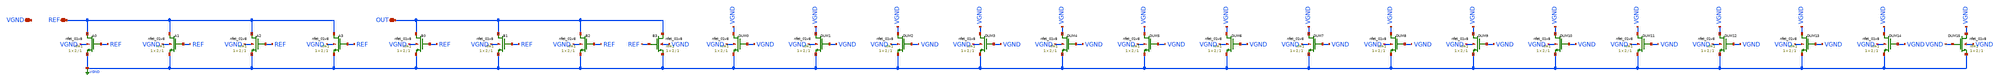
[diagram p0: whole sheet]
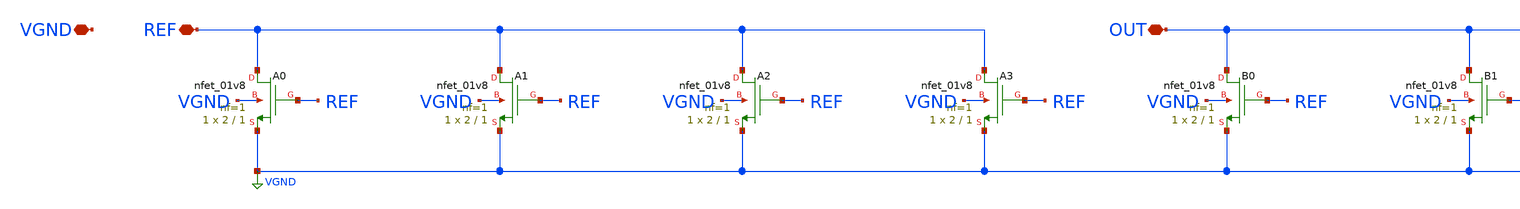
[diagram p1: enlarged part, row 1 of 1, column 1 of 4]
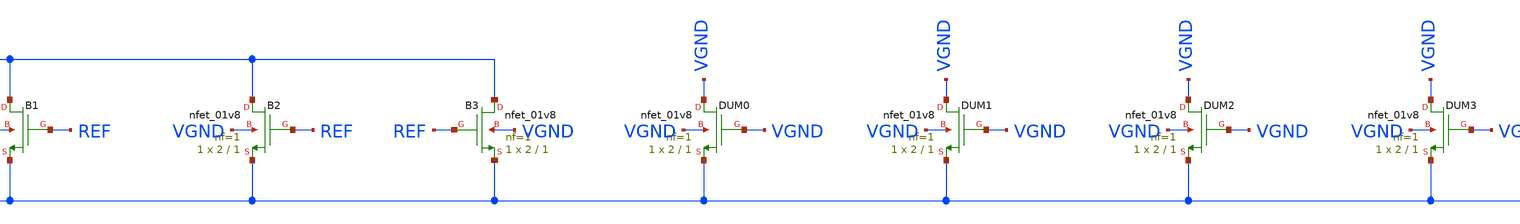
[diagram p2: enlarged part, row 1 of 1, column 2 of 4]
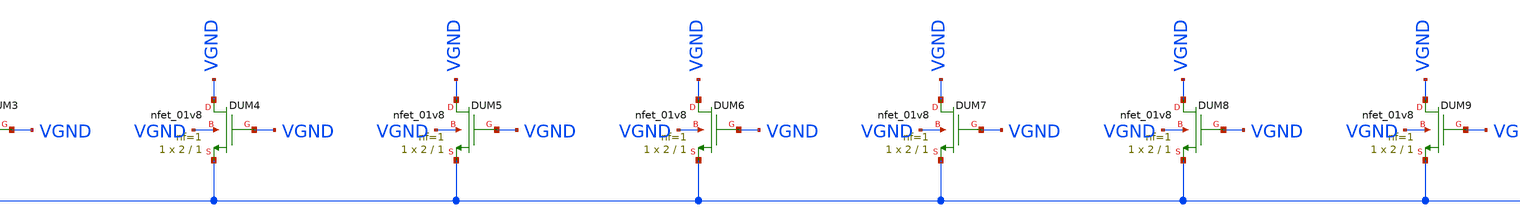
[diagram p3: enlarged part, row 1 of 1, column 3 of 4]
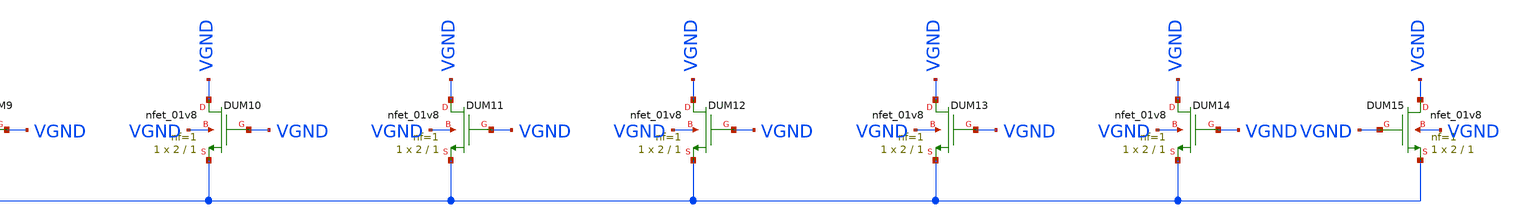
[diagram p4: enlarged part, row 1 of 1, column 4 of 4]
** sch_path: cells/ELAD1_MIRROR_GROUPED/schematic/ELAD1_MIRROR_GROUPED.sch
**.subckt ELAD1_MIRROR_GROUPED REF OUT VGND
*.iopin REF
*.iopin OUT
*.iopin VGND
XA0 REF REF VGND VGND sky130_fd_pr__nfet_01v8 L=1 W=2 nf=1 ad='int((1 + 1)/2) * 2 / 1 * 0.29' as='int((1 + 2)/2) * 2 / 1 * 0.29'
+ pd='2*int((1 + 1)/2) * (2 / 1 + 0.29)' ps='2*int((1 + 2)/2) * (2 / 1 + 0.29)' nrd='0.29 / 2 ' nrs='0.29 / 2 '
+ sa=0 sb=0 sd=0 mult=1 m=1
XA1 REF REF VGND VGND sky130_fd_pr__nfet_01v8 L=1 W=2 nf=1 ad='int((1 + 1)/2) * 2 / 1 * 0.29' as='int((1 + 2)/2) * 2 / 1 * 0.29'
+ pd='2*int((1 + 1)/2) * (2 / 1 + 0.29)' ps='2*int((1 + 2)/2) * (2 / 1 + 0.29)' nrd='0.29 / 2 ' nrs='0.29 / 2 '
+ sa=0 sb=0 sd=0 mult=1 m=1
XA2 REF REF VGND VGND sky130_fd_pr__nfet_01v8 L=1 W=2 nf=1 ad='int((1 + 1)/2) * 2 / 1 * 0.29' as='int((1 + 2)/2) * 2 / 1 * 0.29'
+ pd='2*int((1 + 1)/2) * (2 / 1 + 0.29)' ps='2*int((1 + 2)/2) * (2 / 1 + 0.29)' nrd='0.29 / 2 ' nrs='0.29 / 2 '
+ sa=0 sb=0 sd=0 mult=1 m=1
XA3 REF REF VGND VGND sky130_fd_pr__nfet_01v8 L=1 W=2 nf=1 ad='int((1 + 1)/2) * 2 / 1 * 0.29' as='int((1 + 2)/2) * 2 / 1 * 0.29'
+ pd='2*int((1 + 1)/2) * (2 / 1 + 0.29)' ps='2*int((1 + 2)/2) * (2 / 1 + 0.29)' nrd='0.29 / 2 ' nrs='0.29 / 2 '
+ sa=0 sb=0 sd=0 mult=1 m=1
XB0 OUT REF VGND VGND sky130_fd_pr__nfet_01v8 L=1 W=2 nf=1 ad='int((1 + 1)/2) * 2 / 1 * 0.29' as='int((1 + 2)/2) * 2 / 1 * 0.29'
+ pd='2*int((1 + 1)/2) * (2 / 1 + 0.29)' ps='2*int((1 + 2)/2) * (2 / 1 + 0.29)' nrd='0.29 / 2 ' nrs='0.29 / 2 '
+ sa=0 sb=0 sd=0 mult=1 m=1
XB1 OUT REF VGND VGND sky130_fd_pr__nfet_01v8 L=1 W=2 nf=1 ad='int((1 + 1)/2) * 2 / 1 * 0.29' as='int((1 + 2)/2) * 2 / 1 * 0.29'
+ pd='2*int((1 + 1)/2) * (2 / 1 + 0.29)' ps='2*int((1 + 2)/2) * (2 / 1 + 0.29)' nrd='0.29 / 2 ' nrs='0.29 / 2 '
+ sa=0 sb=0 sd=0 mult=1 m=1
XB2 OUT REF VGND VGND sky130_fd_pr__nfet_01v8 L=1 W=2 nf=1 ad='int((1 + 1)/2) * 2 / 1 * 0.29' as='int((1 + 2)/2) * 2 / 1 * 0.29'
+ pd='2*int((1 + 1)/2) * (2 / 1 + 0.29)' ps='2*int((1 + 2)/2) * (2 / 1 + 0.29)' nrd='0.29 / 2 ' nrs='0.29 / 2 '
+ sa=0 sb=0 sd=0 mult=1 m=1
XB3 OUT REF VGND VGND sky130_fd_pr__nfet_01v8 L=1 W=2 nf=1 ad='int((1 + 1)/2) * 2 / 1 * 0.29' as='int((1 + 2)/2) * 2 / 1 * 0.29'
+ pd='2*int((1 + 1)/2) * (2 / 1 + 0.29)' ps='2*int((1 + 2)/2) * (2 / 1 + 0.29)' nrd='0.29 / 2 ' nrs='0.29 / 2 '
+ sa=0 sb=0 sd=0 mult=1 m=1
XDUM0 VGND VGND VGND VGND sky130_fd_pr__nfet_01v8 L=1 W=2 nf=1 ad='int((1 + 1)/2) * 2 / 1 * 0.29' as='int((1 + 2)/2) * 2 / 1 * 0.29'
+ pd='2*int((1 + 1)/2) * (2 / 1 + 0.29)' ps='2*int((1 + 2)/2) * (2 / 1 + 0.29)' nrd='0.29 / 2 ' nrs='0.29 / 2 '
+ sa=0 sb=0 sd=0 mult=1 m=1
XDUM1 VGND VGND VGND VGND sky130_fd_pr__nfet_01v8 L=1 W=2 nf=1 ad='int((1 + 1)/2) * 2 / 1 * 0.29' as='int((1 + 2)/2) * 2 / 1 * 0.29'
+ pd='2*int((1 + 1)/2) * (2 / 1 + 0.29)' ps='2*int((1 + 2)/2) * (2 / 1 + 0.29)' nrd='0.29 / 2 ' nrs='0.29 / 2 '
+ sa=0 sb=0 sd=0 mult=1 m=1
XDUM2 VGND VGND VGND VGND sky130_fd_pr__nfet_01v8 L=1 W=2 nf=1 ad='int((1 + 1)/2) * 2 / 1 * 0.29' as='int((1 + 2)/2) * 2 / 1 * 0.29'
+ pd='2*int((1 + 1)/2) * (2 / 1 + 0.29)' ps='2*int((1 + 2)/2) * (2 / 1 + 0.29)' nrd='0.29 / 2 ' nrs='0.29 / 2 '
+ sa=0 sb=0 sd=0 mult=1 m=1
XDUM3 VGND VGND VGND VGND sky130_fd_pr__nfet_01v8 L=1 W=2 nf=1 ad='int((1 + 1)/2) * 2 / 1 * 0.29' as='int((1 + 2)/2) * 2 / 1 * 0.29'
+ pd='2*int((1 + 1)/2) * (2 / 1 + 0.29)' ps='2*int((1 + 2)/2) * (2 / 1 + 0.29)' nrd='0.29 / 2 ' nrs='0.29 / 2 '
+ sa=0 sb=0 sd=0 mult=1 m=1
XDUM4 VGND VGND VGND VGND sky130_fd_pr__nfet_01v8 L=1 W=2 nf=1 ad='int((1 + 1)/2) * 2 / 1 * 0.29' as='int((1 + 2)/2) * 2 / 1 * 0.29'
+ pd='2*int((1 + 1)/2) * (2 / 1 + 0.29)' ps='2*int((1 + 2)/2) * (2 / 1 + 0.29)' nrd='0.29 / 2 ' nrs='0.29 / 2 '
+ sa=0 sb=0 sd=0 mult=1 m=1
XDUM5 VGND VGND VGND VGND sky130_fd_pr__nfet_01v8 L=1 W=2 nf=1 ad='int((1 + 1)/2) * 2 / 1 * 0.29' as='int((1 + 2)/2) * 2 / 1 * 0.29'
+ pd='2*int((1 + 1)/2) * (2 / 1 + 0.29)' ps='2*int((1 + 2)/2) * (2 / 1 + 0.29)' nrd='0.29 / 2 ' nrs='0.29 / 2 '
+ sa=0 sb=0 sd=0 mult=1 m=1
XDUM6 VGND VGND VGND VGND sky130_fd_pr__nfet_01v8 L=1 W=2 nf=1 ad='int((1 + 1)/2) * 2 / 1 * 0.29' as='int((1 + 2)/2) * 2 / 1 * 0.29'
+ pd='2*int((1 + 1)/2) * (2 / 1 + 0.29)' ps='2*int((1 + 2)/2) * (2 / 1 + 0.29)' nrd='0.29 / 2 ' nrs='0.29 / 2 '
+ sa=0 sb=0 sd=0 mult=1 m=1
XDUM7 VGND VGND VGND VGND sky130_fd_pr__nfet_01v8 L=1 W=2 nf=1 ad='int((1 + 1)/2) * 2 / 1 * 0.29' as='int((1 + 2)/2) * 2 / 1 * 0.29'
+ pd='2*int((1 + 1)/2) * (2 / 1 + 0.29)' ps='2*int((1 + 2)/2) * (2 / 1 + 0.29)' nrd='0.29 / 2 ' nrs='0.29 / 2 '
+ sa=0 sb=0 sd=0 mult=1 m=1
XDUM8 VGND VGND VGND VGND sky130_fd_pr__nfet_01v8 L=1 W=2 nf=1 ad='int((1 + 1)/2) * 2 / 1 * 0.29' as='int((1 + 2)/2) * 2 / 1 * 0.29'
+ pd='2*int((1 + 1)/2) * (2 / 1 + 0.29)' ps='2*int((1 + 2)/2) * (2 / 1 + 0.29)' nrd='0.29 / 2 ' nrs='0.29 / 2 '
+ sa=0 sb=0 sd=0 mult=1 m=1
XDUM9 VGND VGND VGND VGND sky130_fd_pr__nfet_01v8 L=1 W=2 nf=1 ad='int((1 + 1)/2) * 2 / 1 * 0.29' as='int((1 + 2)/2) * 2 / 1 * 0.29'
+ pd='2*int((1 + 1)/2) * (2 / 1 + 0.29)' ps='2*int((1 + 2)/2) * (2 / 1 + 0.29)' nrd='0.29 / 2 ' nrs='0.29 / 2 '
+ sa=0 sb=0 sd=0 mult=1 m=1
XDUM10 VGND VGND VGND VGND sky130_fd_pr__nfet_01v8 L=1 W=2 nf=1 ad='int((1 + 1)/2) * 2 / 1 * 0.29' as='int((1 + 2)/2) * 2 / 1 * 0.29'
+ pd='2*int((1 + 1)/2) * (2 / 1 + 0.29)' ps='2*int((1 + 2)/2) * (2 / 1 + 0.29)' nrd='0.29 / 2 ' nrs='0.29 / 2 '
+ sa=0 sb=0 sd=0 mult=1 m=1
XDUM11 VGND VGND VGND VGND sky130_fd_pr__nfet_01v8 L=1 W=2 nf=1 ad='int((1 + 1)/2) * 2 / 1 * 0.29' as='int((1 + 2)/2) * 2 / 1 * 0.29'
+ pd='2*int((1 + 1)/2) * (2 / 1 + 0.29)' ps='2*int((1 + 2)/2) * (2 / 1 + 0.29)' nrd='0.29 / 2 ' nrs='0.29 / 2 '
+ sa=0 sb=0 sd=0 mult=1 m=1
XDUM12 VGND VGND VGND VGND sky130_fd_pr__nfet_01v8 L=1 W=2 nf=1 ad='int((1 + 1)/2) * 2 / 1 * 0.29' as='int((1 + 2)/2) * 2 / 1 * 0.29'
+ pd='2*int((1 + 1)/2) * (2 / 1 + 0.29)' ps='2*int((1 + 2)/2) * (2 / 1 + 0.29)' nrd='0.29 / 2 ' nrs='0.29 / 2 '
+ sa=0 sb=0 sd=0 mult=1 m=1
XDUM13 VGND VGND VGND VGND sky130_fd_pr__nfet_01v8 L=1 W=2 nf=1 ad='int((1 + 1)/2) * 2 / 1 * 0.29' as='int((1 + 2)/2) * 2 / 1 * 0.29'
+ pd='2*int((1 + 1)/2) * (2 / 1 + 0.29)' ps='2*int((1 + 2)/2) * (2 / 1 + 0.29)' nrd='0.29 / 2 ' nrs='0.29 / 2 '
+ sa=0 sb=0 sd=0 mult=1 m=1
XDUM14 VGND VGND VGND VGND sky130_fd_pr__nfet_01v8 L=1 W=2 nf=1 ad='int((1 + 1)/2) * 2 / 1 * 0.29' as='int((1 + 2)/2) * 2 / 1 * 0.29'
+ pd='2*int((1 + 1)/2) * (2 / 1 + 0.29)' ps='2*int((1 + 2)/2) * (2 / 1 + 0.29)' nrd='0.29 / 2 ' nrs='0.29 / 2 '
+ sa=0 sb=0 sd=0 mult=1 m=1
XDUM15 VGND VGND VGND VGND sky130_fd_pr__nfet_01v8 L=1 W=2 nf=1 ad='int((1 + 1)/2) * 2 / 1 * 0.29' as='int((1 + 2)/2) * 2 / 1 * 0.29'
+ pd='2*int((1 + 1)/2) * (2 / 1 + 0.29)' ps='2*int((1 + 2)/2) * (2 / 1 + 0.29)' nrd='0.29 / 2 ' nrs='0.29 / 2 '
+ sa=0 sb=0 sd=0 mult=1 m=1
**.ends
.GLOBAL VGND
.end
